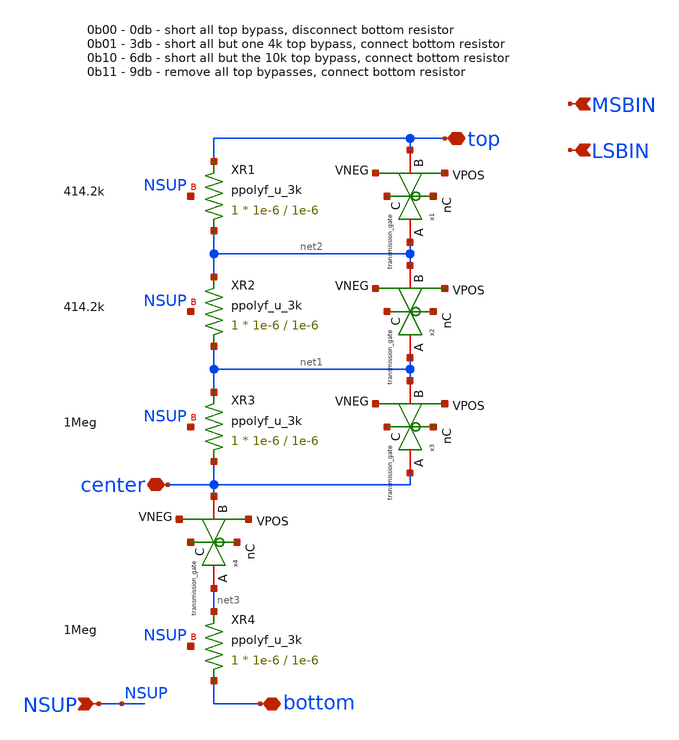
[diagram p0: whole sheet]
** sch_path: xschem/blocks/rdiv_0_9_3db/rdiv_0_9_3db.sch
**.subckt rdiv_0_9_3db top center bottom MSBIN LSBIN NSUP
*.iopin top
*.iopin center
*.iopin bottom
*.ipin MSBIN
*.ipin LSBIN
*.ipin NSUP
XR1 net2 top NSUP ppolyf_u_3k r_width=1e-6 r_length=1e-6 m=1
XR2 net1 net2 NSUP ppolyf_u_3k r_width=1e-6 r_length=1e-6 m=1
XR3 center net1 NSUP ppolyf_u_3k r_width=1e-6 r_length=1e-6 m=1
XR4 bottom net3 NSUP ppolyf_u_3k r_width=1e-6 r_length=1e-6 m=1
x1 net4 net2 top net5 net6 net7 transmission_gate
x2 net8 net1 net2 net9 net10 net11 transmission_gate
x3 net12 center net1 net13 net14 net15 transmission_gate
x4 net16 net3 center net17 net18 net19 transmission_gate
**.ends

* expanding   symbol:  blocks/transmission_gate/transmission_gate.sym # of pins=6
** sym_path: xschem/blocks/transmission_gate/transmission_gate.sym
** sch_path: xschem/blocks/transmission_gate/transmission_gate.sch
.subckt transmission_gate C A B nC VPOS VNEG
*.iopin A
*.iopin B
*.ipin C
*.ipin nC
*.ipin VPOS
*.ipin VNEG
XM1 B C A VNEG nfet_06v0 L=0.70u W=0.30u nf=1 ad='int((nf+1)/2) * W/nf * 0.18u' as='int((nf+2)/2) * W/nf * 0.18u'
+ pd='2*int((nf+1)/2) * (W/nf + 0.18u)' ps='2*int((nf+2)/2) * (W/nf + 0.18u)' nrd='0.18u / W' nrs='0.18u / W'
+ sa=0 sb=0 sd=0 m=1
XM2 A nC B VPOS pfet_06v0 L=0.55u W=0.30u nf=1 ad='int((nf+1)/2) * W/nf * 0.18u' as='int((nf+2)/2) * W/nf * 0.18u'
+ pd='2*int((nf+1)/2) * (W/nf + 0.18u)' ps='2*int((nf+2)/2) * (W/nf + 0.18u)' nrd='0.18u / W' nrs='0.18u / W'
+ sa=0 sb=0 sd=0 m=1
.ends

.end
